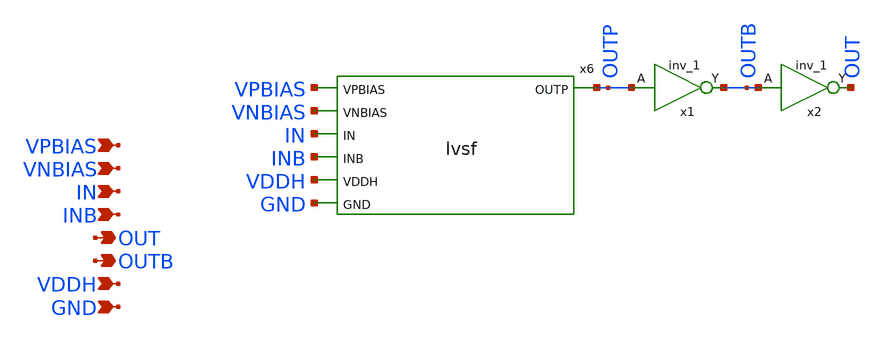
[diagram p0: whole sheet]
** sch_path: xschem/lvsf_1buff.sch
**.subckt lvsf_1buff IN INB OUT VDDH GND VPBIAS VNBIAS OUTB
*.ipin IN
*.ipin INB
*.opin OUT
*.ipin VDDH
*.ipin GND
*.ipin VPBIAS
*.ipin VNBIAS
*.opin OUTB
x1 OUTP GND GND VDDH VDDH OUTB sky130_fd_sc_hvl__inv_1
x2 OUTB GND GND VDDH VDDH OUT sky130_fd_sc_hvl__inv_1
x6 VPBIAS VNBIAS IN INB OUTP VDDH GND lvsf
**.ends

* expanding   symbol:  lvsf.sym # of pins=7
** sym_path: xschem/lvsf.sym
** sch_path: xschem/lvsf.sch
.subckt lvsf VPBIAS VNBIAS IN INB OUTP VDDH GND
*.ipin IN
*.ipin INB
*.opin OUTP
*.ipin VDDH
*.ipin GND
*.ipin VPBIAS
*.ipin VNBIAS
XM1 net1 VPBIAS VDDH VDDH sky130_fd_pr__pfet_g5v0d10v5 L=0.8 W=1 nf=1 ad='int((nf+1)/2) * W/nf * 0.29'
+ as='int((nf+2)/2) * W/nf * 0.29' pd='2*int((nf+1)/2) * (W/nf + 0.29)' ps='2*int((nf+2)/2) * (W/nf + 0.29)'
+ nrd='0.29 / W' nrs='0.29 / W' sa=0 sb=0 sd=0 mult=1 m=1
XM2 net2 VPBIAS VDDH VDDH sky130_fd_pr__pfet_g5v0d10v5 L=0.8 W=1 nf=1 ad='int((nf+1)/2) * W/nf * 0.29'
+ as='int((nf+2)/2) * W/nf * 0.29' pd='2*int((nf+1)/2) * (W/nf + 0.29)' ps='2*int((nf+2)/2) * (W/nf + 0.29)'
+ nrd='0.29 / W' nrs='0.29 / W' sa=0 sb=0 sd=0 mult=1 m=1
XM3 OUTPB OUTP net1 VDDH sky130_fd_pr__pfet_g5v0d10v5 L=0.8 W=1 nf=1 ad='int((nf+1)/2) * W/nf * 0.29'
+ as='int((nf+2)/2) * W/nf * 0.29' pd='2*int((nf+1)/2) * (W/nf + 0.29)' ps='2*int((nf+2)/2) * (W/nf + 0.29)'
+ nrd='0.29 / W' nrs='0.29 / W' sa=0 sb=0 sd=0 mult=1 m=1
XM4 OUTP OUTPB net2 VDDH sky130_fd_pr__pfet_g5v0d10v5 L=0.8 W=1 nf=1 ad='int((nf+1)/2) * W/nf * 0.29'
+ as='int((nf+2)/2) * W/nf * 0.29' pd='2*int((nf+1)/2) * (W/nf + 0.29)' ps='2*int((nf+2)/2) * (W/nf + 0.29)'
+ nrd='0.29 / W' nrs='0.29 / W' sa=0 sb=0 sd=0 mult=1 m=1
XM8 OUTP VNBIAS n2 GND sky130_fd_pr__nfet_g5v0d10v5 L=1 W=1 nf=1 ad='int((nf+1)/2) * W/nf * 0.29' as='int((nf+2)/2) * W/nf * 0.29'
+ pd='2*int((nf+1)/2) * (W/nf + 0.29)' ps='2*int((nf+2)/2) * (W/nf + 0.29)' nrd='0.29 / W' nrs='0.29 / W'
+ sa=0 sb=0 sd=0 mult=1 m=1
XM5 OUTPB VNBIAS n1 GND sky130_fd_pr__nfet_g5v0d10v5 L=1 W=1 nf=1 ad='int((nf+1)/2) * W/nf * 0.29' as='int((nf+2)/2) * W/nf * 0.29'
+ pd='2*int((nf+1)/2) * (W/nf + 0.29)' ps='2*int((nf+2)/2) * (W/nf + 0.29)' nrd='0.29 / W' nrs='0.29 / W'
+ sa=0 sb=0 sd=0 mult=1 m=1
XM6 n1 IN GND GND sky130_fd_pr__nfet_01v8 L=0.15 W=3 nf=1 ad='int((nf+1)/2) * W/nf * 0.29' as='int((nf+2)/2) * W/nf * 0.29'
+ pd='2*int((nf+1)/2) * (W/nf + 0.29)' ps='2*int((nf+2)/2) * (W/nf + 0.29)' nrd='0.29 / W' nrs='0.29 / W'
+ sa=0 sb=0 sd=0 mult=1 m=1
XM7 n2 INB GND GND sky130_fd_pr__nfet_01v8 L=0.15 W=3 nf=1 ad='int((nf+1)/2) * W/nf * 0.29' as='int((nf+2)/2) * W/nf * 0.29'
+ pd='2*int((nf+1)/2) * (W/nf + 0.29)' ps='2*int((nf+2)/2) * (W/nf + 0.29)' nrd='0.29 / W' nrs='0.29 / W'
+ sa=0 sb=0 sd=0 mult=1 m=1
.ends

.end
